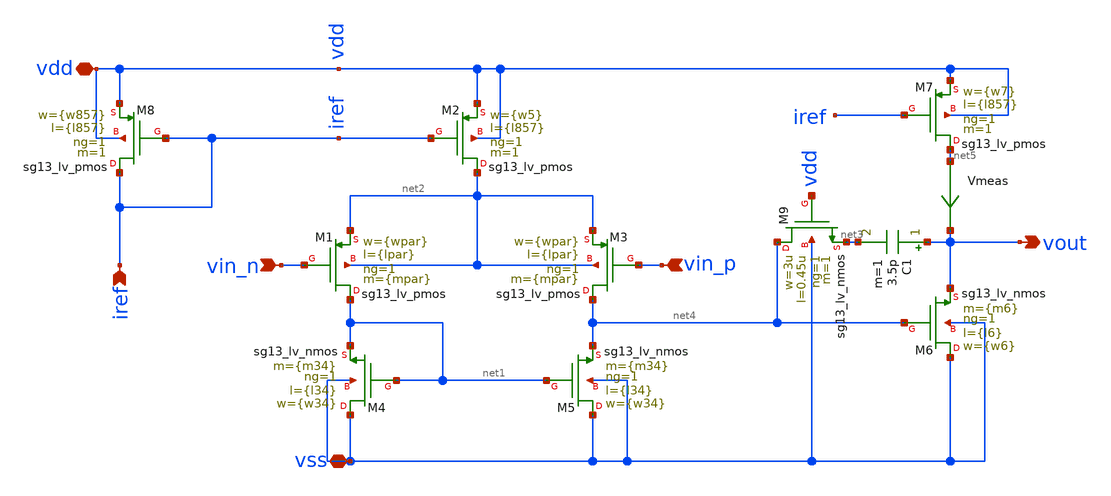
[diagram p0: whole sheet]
** sch_path: ihp_ota.sch
**.subckt ihp_ota vin_n vin_p iref vdd vss vout
*.ipin vin_n
*.ipin vin_p
*.ipin iref
*.iopin vdd
*.iopin vss
*.opin vout
XM2 net2 iref vdd vdd sg13_lv_pmos w={w5} l={l857} ng=1 m=1 mm_ok=1
XM4 vss net1 net1 vss sg13_lv_nmos w={w34} l={l34} ng=1 m={m34} mm_ok=1
XM6 vss net4 vout vss sg13_lv_nmos w={w6} l={l6} ng=1 m={m6} mm_ok=1
XM7 net5 iref vdd vdd sg13_lv_pmos w={w7} l={l857} ng=1 m=1 mm_ok=1
C1 vout net3 3.5p m=1
XM8 iref iref vdd vdd sg13_lv_pmos w={w857} l={l857} ng=1 m=1 mm_ok=1
XM9 net4 vdd net3 vss sg13_lv_nmos w=3u l=0.45u ng=1 m=1 mm_ok=1
XM1 net1 vin_n net2 net2 sg13_lv_pmos w={wpar} l={lpar} ng=1 m={mpar} mm_ok=1
XM3 net4 vin_p net2 net2 sg13_lv_pmos w={wpar} l={lpar} ng=1 m={mpar} mm_ok=1
XM5 vss net1 net4 vss sg13_lv_nmos w={w34} l={l34} ng=1 m={m34} mm_ok=1
Vmeas net5 vout 0
.save i(vmeas)
**.ends
.end
